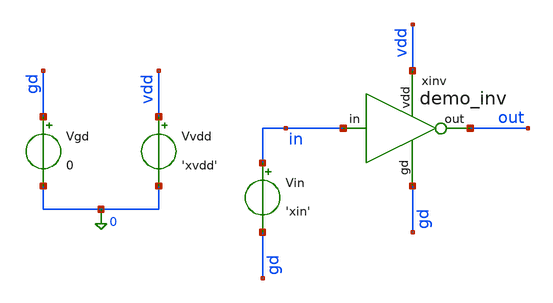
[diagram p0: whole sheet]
** sch_path: analog/klayout/production/final_merge_20260923/testbenches/cace/analog/xschem/tb_demo_inv.sch
**.subckt tb_demo_inv
xinv vdd in out gd demo_inv
Vgd gd 0 0
Vvdd vdd 0 'xvdd'
Vin in gd 'xin'
**.ends

* expanding   symbol:  demo_inv.sym # of pins=4
** sym_path: analog/klayout/production/final_merge_20260923/testbenches/cace/analog/xschem/demo_inv.sym
** sch_path: analog/klayout/production/final_merge_20260923/testbenches/cace/analog/xschem/demo_inv.sch
.subckt demo_inv vdd in out gd
*.ipin in
*.iopin vdd
*.iopin gd
*.opin out
XMn out in gd gd sky130_fd_pr__nfet_01v8 L=0.15 W=1 nf=1 ad='int((1 + 1)/2) * 1 / 1 * 0.29' as='int((1 + 2)/2) * 1 / 1 * 0.29'
+ pd='2*int((1 + 1)/2) * (1 / 1 + 0.29)' ps='2*int((1 + 2)/2) * (1 / 1 + 0.29)' nrd='0.29 / 1 ' nrs='0.29 / 1 '
+ sa=0 sb=0 sd=0 mult=1 m=1
XMp out in vdd vdd sky130_fd_pr__pfet_01v8 L=0.15 W=1 nf=1 ad='int((1 + 1)/2) * 1 / 1 * 0.29' as='int((1 + 2)/2) * 1 / 1 * 0.29'
+ pd='2*int((1 + 1)/2) * (1 / 1 + 0.29)' ps='2*int((1 + 2)/2) * (1 / 1 + 0.29)' nrd='0.29 / 1 ' nrs='0.29 / 1 '
+ sa=0 sb=0 sd=0 mult=1 m=1
.ends

.end
